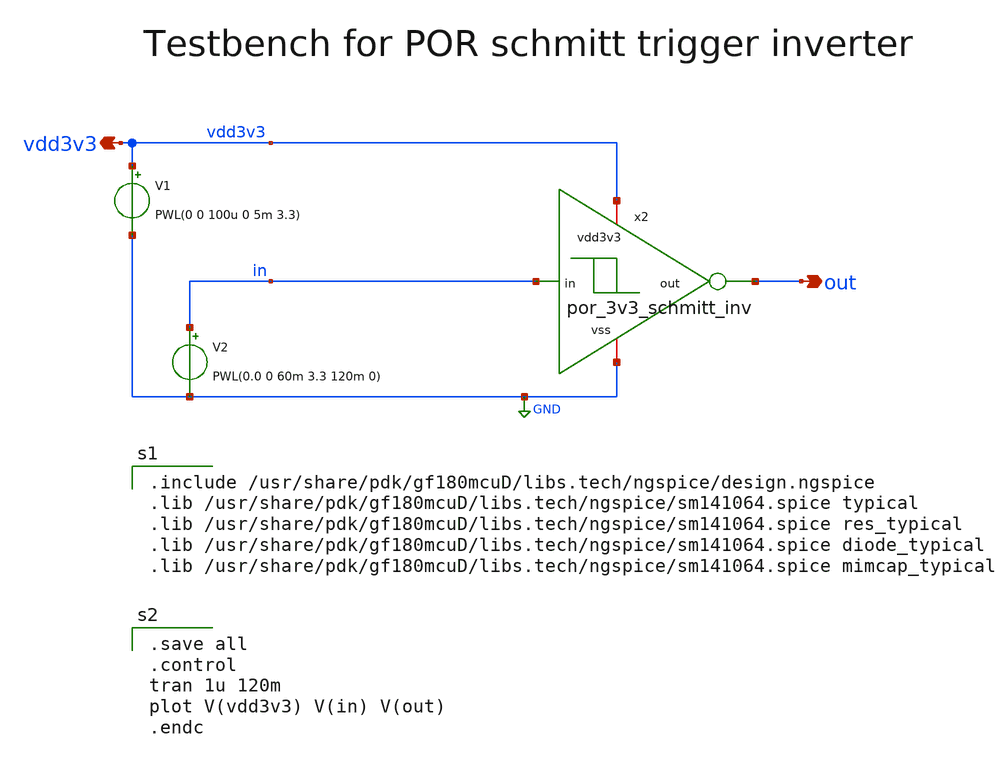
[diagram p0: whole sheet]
** sch_path: projects/programmable_transceiver_platform/analog/core_support/por/xschem/schmitt_tb.sch
**.subckt schmitt_tb vdd3v3 out
*.opin vdd3v3
*.opin out
V1 vdd3v3 GND PWL(0 0 100u 0 5m 3.3)
V2 in GND PWL(0.0 0 60m 3.3 120m 0)
x2 vdd3v3 in out GND por_3v3_schmitt_inv
**** begin user architecture code

.save all
.control
tran 1u 120m
plot V(vdd3v3) V(in) V(out)
.endc


.include /usr/share/pdk/gf180mcuD/libs.tech/ngspice/design.ngspice
.lib /usr/share/pdk/gf180mcuD/libs.tech/ngspice/sm141064.spice typical
.lib /usr/share/pdk/gf180mcuD/libs.tech/ngspice/sm141064.spice res_typical
.lib /usr/share/pdk/gf180mcuD/libs.tech/ngspice/sm141064.spice diode_typical
.lib /usr/share/pdk/gf180mcuD/libs.tech/ngspice/sm141064.spice mimcap_typical

**** end user architecture code
**.ends

* expanding   symbol:  por_3v3_schmitt_inv.sym # of pins=4
** sym_path: projects/programmable_transceiver_platform/analog/core_support/por/xschem/por_3v3_schmitt_inv.sym
** sch_path: projects/programmable_transceiver_platform/analog/core_support/por/xschem/por_3v3_schmitt_inv.sch
.subckt por_3v3_schmitt_inv vdd3v3 in out vss
*.iopin vdd3v3
*.iopin vss
*.ipin in
*.opin out
XM1 out in n1 vss nfet_03v3 L=0.28u W=1.5u nf=2 ad='int((nf+1)/2) * W/nf * 0.18u' as='int((nf+2)/2) * W/nf * 0.18u'
+ pd='2*int((nf+1)/2) * (W/nf + 0.18u)' ps='2*int((nf+2)/2) * (W/nf + 0.18u)' nrd='0.18u / W' nrs='0.18u / W'
+ sa=0 sb=0 sd=0 m=1
XM2 out in p1 vdd3v3 pfet_03v3 L=0.28u W=0.75u nf=1 ad='int((nf+1)/2) * W/nf * 0.18u' as='int((nf+2)/2) * W/nf * 0.18u'
+ pd='2*int((nf+1)/2) * (W/nf + 0.18u)' ps='2*int((nf+2)/2) * (W/nf + 0.18u)' nrd='0.18u / W' nrs='0.18u / W'
+ sa=0 sb=0 sd=0 m=1
XM3 p1 in vdd3v3 vdd3v3 pfet_03v3 L=0.28u W=3u nf=4 ad='int((nf+1)/2) * W/nf * 0.18u' as='int((nf+2)/2) * W/nf * 0.18u'
+ pd='2*int((nf+1)/2) * (W/nf + 0.18u)' ps='2*int((nf+2)/2) * (W/nf + 0.18u)' nrd='0.18u / W' nrs='0.18u / W'
+ sa=0 sb=0 sd=0 m=1
XM4 n1 in vss vss nfet_03v3 L=0.28u W=1.5u nf=2 ad='int((nf+1)/2) * W/nf * 0.18u' as='int((nf+2)/2) * W/nf * 0.18u'
+ pd='2*int((nf+1)/2) * (W/nf + 0.18u)' ps='2*int((nf+2)/2) * (W/nf + 0.18u)' nrd='0.18u / W' nrs='0.18u / W'
+ sa=0 sb=0 sd=0 m=1
XM5 n1 out vdd3v3 vss nfet_03v3 L=0.56u W=6u nf=1 ad='int((nf+1)/2) * W/nf * 0.18u' as='int((nf+2)/2) * W/nf * 0.18u'
+ pd='2*int((nf+1)/2) * (W/nf + 0.18u)' ps='2*int((nf+2)/2) * (W/nf + 0.18u)' nrd='0.18u / W' nrs='0.18u / W'
+ sa=0 sb=0 sd=0 m=1
XM6 p1 out vss vdd3v3 pfet_03v3 L=0.56u W=3u nf=1 ad='int((nf+1)/2) * W/nf * 0.18u' as='int((nf+2)/2) * W/nf * 0.18u'
+ pd='2*int((nf+1)/2) * (W/nf + 0.18u)' ps='2*int((nf+2)/2) * (W/nf + 0.18u)' nrd='0.18u / W' nrs='0.18u / W'
+ sa=0 sb=0 sd=0 m=1
.ends

.GLOBAL GND
.end
